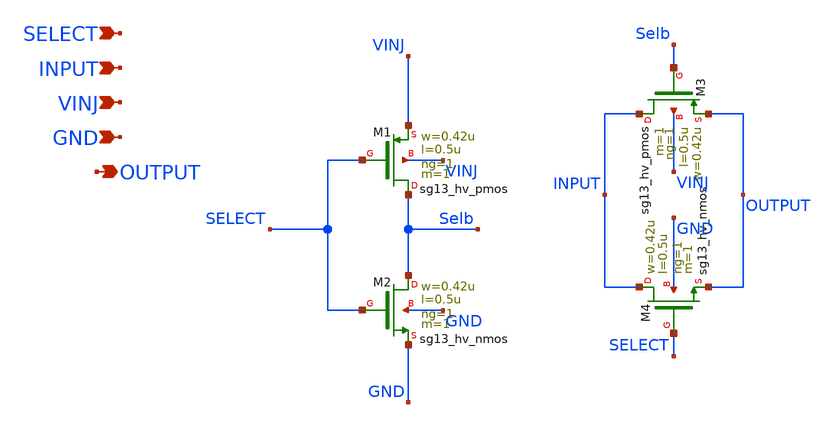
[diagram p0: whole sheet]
** sch_path: ihp130_cells/TgateVinj02/ihp130_TgateVinj02.sch
**.subckt ihp130_TgateVinj02 SELECT INPUT VINJ GND OUTPUT
*.ipin SELECT
*.ipin INPUT
*.ipin VINJ
*.ipin GND
*.opin OUTPUT
XM1 Selb SELECT VINJ VINJ sg13_hv_pmos w=0.42u l=0.5u ng=1 m=1 mm_ok=1
XM2 Selb SELECT GND GND sg13_hv_nmos w=0.42u l=0.5u ng=1 m=1 mm_ok=1
XM3 INPUT Selb OUTPUT VINJ sg13_hv_pmos w=0.42u l=0.5u ng=1 m=1 mm_ok=1
XM4 INPUT SELECT OUTPUT GND sg13_hv_nmos w=0.42u l=0.5u ng=1 m=1 mm_ok=1
**.ends
.end
